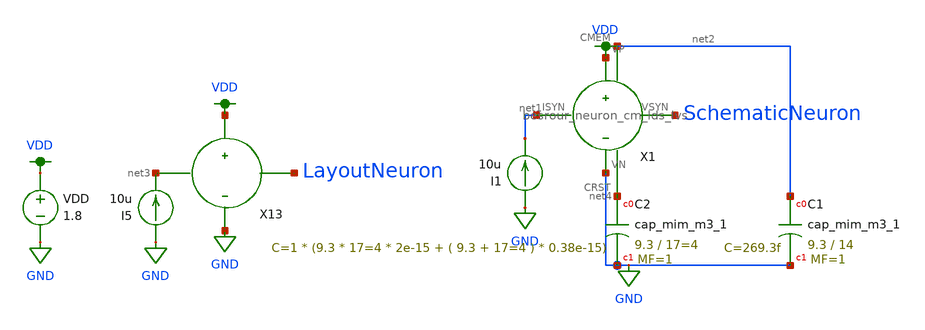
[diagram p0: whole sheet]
** sch_path: schematic/neuron.sch
**.subckt neuron
X13 net3 LayoutNeuron VDD GND neuron_top
I5 GND net3 10u
VDD VDD GND 1.8
X1 net1 SchematicNeuron VDD GND net2 net4 besrour_neuron_cm_lds_lvs
I1 GND net1 10u
XC1 net2 GND sky130_fd_pr__cap_mim_m3_1 W=9.3 L=14 MF=1 m=1
XC2 net4 GND sky130_fd_pr__cap_mim_m3_1 W=9.3 L=17=4 MF=1 m=1
**** begin user architecture code

.param W=2
.param L=0.3
.include ~/neuromorphic_computing_final/schematic/memristor_emulator_res.spice
.include ~/neuromorphic_computing_final/schematic/neuron_top.spice
.tran 0.5ns 2us
.save all


.option wnflag=1
.param MC_SWITCH=0.0
.lib ~/skywater/skywater-pdk/libraries/sky130_fd_pr_ngspice/latest/models/sky130.lib.spice tt

**** end user architecture code
**.ends

* expanding   symbol:
*+  /home/madvlsi/neuromorphic_computing_final/schematic/besrour_neuron_cm_lds_lvs.sym # of pins=6
** sym_path: schematic/besrour_neuron_cm_lds_lvs.sym
** sch_path: schematic/besrour_neuron_cm_lds_lvs.sch
.subckt besrour_neuron_cm_lds_lvs ISYN VSYN VP VN CMEM CRST
*.iopin VP
*.iopin VN
*.iopin ISYN
*.opin VSYN
*.opin CMEM
*.opin CRST
XM15 VP net1 net1 VP sky130_fd_pr__pfet_01v8 L=0.3 W=2 nf=1 ad='int((nf+1)/2) * W/nf * 0.29' as='int((nf+2)/2) * W/nf * 0.29'
+ pd='2*int((nf+1)/2) * (W/nf + 0.29)' ps='2*int((nf+2)/2) * (W/nf + 0.29)' nrd='0.29 / W' nrs='0.29 / W'
+ sa=0 sb=0 sd=0 mult=1 m=1
XM17 VN ISYN net1 VN sky130_fd_pr__nfet_01v8 L=0.3 W=2 nf=1 ad='int((nf+1)/2) * W/nf * 0.29' as='int((nf+2)/2) * W/nf * 0.29'
+ pd='2*int((nf+1)/2) * (W/nf + 0.29)' ps='2*int((nf+2)/2) * (W/nf + 0.29)' nrd='0.29 / W' nrs='0.29 / W'
+ sa=0 sb=0 sd=0 mult=1 m=1
XM7 ISYN ISYN VN VN sky130_fd_pr__nfet_01v8 L=0.3 W=2 nf=1 ad='int((nf+1)/2) * W/nf * 0.29' as='int((nf+2)/2) * W/nf * 0.29'
+ pd='2*int((nf+1)/2) * (W/nf + 0.29)' ps='2*int((nf+2)/2) * (W/nf + 0.29)' nrd='0.29 / W' nrs='0.29 / W'
+ sa=0 sb=0 sd=0 mult=1 m=1
XM8 VN CRST CMEM VN sky130_fd_pr__nfet_01v8 L=0.3 W=2 nf=1 ad='int((nf+1)/2) * W/nf * 0.29' as='int((nf+2)/2) * W/nf * 0.29'
+ pd='2*int((nf+1)/2) * (W/nf + 0.29)' ps='2*int((nf+2)/2) * (W/nf + 0.29)' nrd='0.29 / W' nrs='0.29 / W'
+ sa=0 sb=0 sd=0 mult=1 m=1
XM9 net2 CMEM VN VN sky130_fd_pr__nfet_01v8 L=0.3 W=2 nf=1 ad='int((nf+1)/2) * W/nf * 0.29' as='int((nf+2)/2) * W/nf * 0.29'
+ pd='2*int((nf+1)/2) * (W/nf + 0.29)' ps='2*int((nf+2)/2) * (W/nf + 0.29)' nrd='0.29 / W' nrs='0.29 / W'
+ sa=0 sb=0 sd=0 mult=1 m=1
XM10 VN net2 CRST VN sky130_fd_pr__nfet_01v8 L=0.3 W=2 nf=1 ad='int((nf+1)/2) * W/nf * 0.29' as='int((nf+2)/2) * W/nf * 0.29'
+ pd='2*int((nf+1)/2) * (W/nf + 0.29)' ps='2*int((nf+2)/2) * (W/nf + 0.29)' nrd='0.29 / W' nrs='0.29 / W'
+ sa=0 sb=0 sd=0 mult=1 m=1
XM11 net3 CRST VN VN sky130_fd_pr__nfet_01v8 L=0.3 W=2 nf=1 ad='int((nf+1)/2) * W/nf * 0.29' as='int((nf+2)/2) * W/nf * 0.29'
+ pd='2*int((nf+1)/2) * (W/nf + 0.29)' ps='2*int((nf+2)/2) * (W/nf + 0.29)' nrd='0.29 / W' nrs='0.29 / W'
+ sa=0 sb=0 sd=0 mult=1 m=1
XM12 VSYN net3 VN VN sky130_fd_pr__nfet_01v8 L=0.3 W=2 nf=1 ad='int((nf+1)/2) * W/nf * 0.29' as='int((nf+2)/2) * W/nf * 0.29'
+ pd='2*int((nf+1)/2) * (W/nf + 0.29)' ps='2*int((nf+2)/2) * (W/nf + 0.29)' nrd='0.29 / W' nrs='0.29 / W'
+ sa=0 sb=0 sd=0 mult=1 m=1
XM1 CMEM net1 VP VP sky130_fd_pr__pfet_01v8 L=0.3 W=2 nf=1 ad='int((nf+1)/2) * W/nf * 0.29' as='int((nf+2)/2) * W/nf * 0.29'
+ pd='2*int((nf+1)/2) * (W/nf + 0.29)' ps='2*int((nf+2)/2) * (W/nf + 0.29)' nrd='0.29 / W' nrs='0.29 / W'
+ sa=0 sb=0 sd=0 mult=1 m=1
XM2 VP net2 CMEM VP sky130_fd_pr__pfet_01v8 L=0.3 W=2 nf=1 ad='int((nf+1)/2) * W/nf * 0.29' as='int((nf+2)/2) * W/nf * 0.29'
+ pd='2*int((nf+1)/2) * (W/nf + 0.29)' ps='2*int((nf+2)/2) * (W/nf + 0.29)' nrd='0.29 / W' nrs='0.29 / W'
+ sa=0 sb=0 sd=0 mult=1 m=1
XM3 net2 CMEM VP VP sky130_fd_pr__pfet_01v8 L=0.3 W=2 nf=1 ad='int((nf+1)/2) * W/nf * 0.29' as='int((nf+2)/2) * W/nf * 0.29'
+ pd='2*int((nf+1)/2) * (W/nf + 0.29)' ps='2*int((nf+2)/2) * (W/nf + 0.29)' nrd='0.29 / W' nrs='0.29 / W'
+ sa=0 sb=0 sd=0 mult=1 m=1
XM4 VP net2 CRST VP sky130_fd_pr__pfet_01v8 L=0.3 W=2 nf=1 ad='int((nf+1)/2) * W/nf * 0.29' as='int((nf+2)/2) * W/nf * 0.29'
+ pd='2*int((nf+1)/2) * (W/nf + 0.29)' ps='2*int((nf+2)/2) * (W/nf + 0.29)' nrd='0.29 / W' nrs='0.29 / W'
+ sa=0 sb=0 sd=0 mult=1 m=1
XM5 net3 CRST VP VP sky130_fd_pr__pfet_01v8 L=0.3 W=2 nf=1 ad='int((nf+1)/2) * W/nf * 0.29' as='int((nf+2)/2) * W/nf * 0.29'
+ pd='2*int((nf+1)/2) * (W/nf + 0.29)' ps='2*int((nf+2)/2) * (W/nf + 0.29)' nrd='0.29 / W' nrs='0.29 / W'
+ sa=0 sb=0 sd=0 mult=1 m=1
XM6 VSYN net3 VP VP sky130_fd_pr__pfet_01v8 L=0.3 W=2 nf=1 ad='int((nf+1)/2) * W/nf * 0.29' as='int((nf+2)/2) * W/nf * 0.29'
+ pd='2*int((nf+1)/2) * (W/nf + 0.29)' ps='2*int((nf+2)/2) * (W/nf + 0.29)' nrd='0.29 / W' nrs='0.29 / W'
+ sa=0 sb=0 sd=0 mult=1 m=1
.ends

.GLOBAL VDD
.GLOBAL GND
.end
